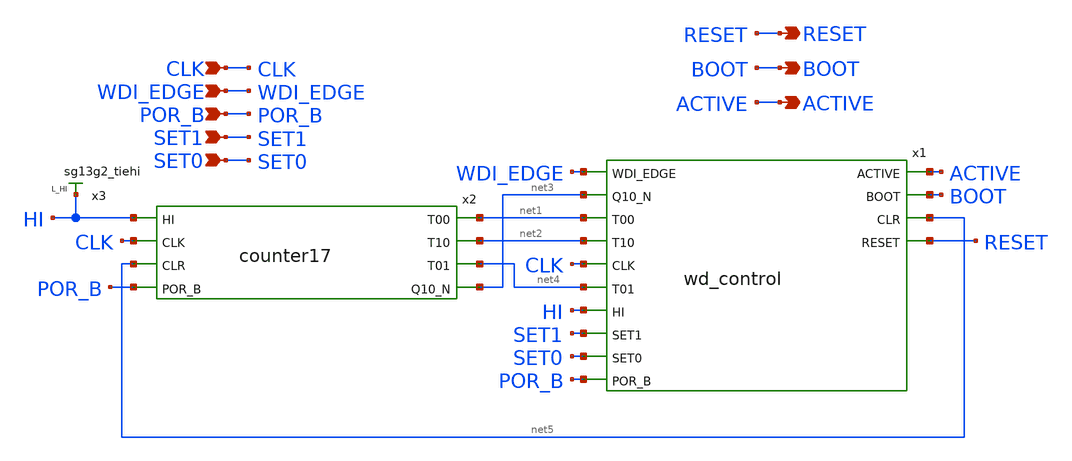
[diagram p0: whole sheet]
** sch_path: design/blocks/digital/schematic/wd_digital.sch
**.subckt wd_digital ACTIVE CLK WDI_EDGE BOOT RESET POR_B SET1 SET0
*.opin ACTIVE
*.ipin CLK
*.ipin WDI_EDGE
*.opin BOOT
*.opin RESET
*.ipin POR_B
*.ipin SET1
*.ipin SET0
x1 WDI_EDGE net3 net1 net2 CLK net4 HI ACTIVE SET1 BOOT net5 SET0 RESET POR_B VDD VSS wd_control
x2 net1 HI net2 CLK net5 net4 net3 POR_B VDD VSS counter17
x3 HI VDD VSS sg13g2_tiehi
**.ends
.end
